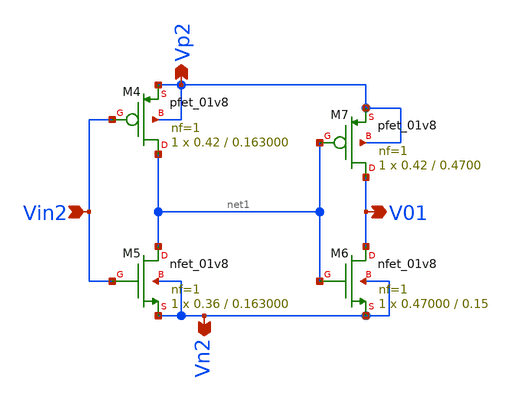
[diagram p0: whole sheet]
** sch_path: xschem/Vth_sch/Symbol/th01_2.sch
**.subckt th01_2 Vn2 Vp2 Vin2 V01
*.opin Vn2
*.opin Vp2
*.ipin Vin2
*.opin V01
XM7 V01 net1 Vp2 Vp2 sky130_fd_pr__pfet_01v8 L=0.4700 W=0.42 nf=1 ad='int((nf+1)/2) * W/nf * 0.29' as='int((nf+2)/2) * W/nf * 0.29'
+ pd='2*int((nf+1)/2) * (W/nf + 0.29)' ps='2*int((nf+2)/2) * (W/nf + 0.29)' nrd='0.29 / W' nrs='0.29 / W'
+ sa=0 sb=0 sd=0 mult=1 m=1
XM6 V01 net1 Vn2 Vn2 sky130_fd_pr__nfet_01v8 L=0.15 W=0.47000 nf=1 ad='int((nf+1)/2) * W/nf * 0.29' as='int((nf+2)/2) * W/nf * 0.29'
+ pd='2*int((nf+1)/2) * (W/nf + 0.29)' ps='2*int((nf+2)/2) * (W/nf + 0.29)' nrd='0.29 / W' nrs='0.29 / W'
+ sa=0 sb=0 sd=0 mult=1 m=1
XM4 net1 Vin2 Vp2 Vp2 sky130_fd_pr__pfet_01v8 L=0.163000 W=0.42 nf=1 ad='int((nf+1)/2) * W/nf * 0.29'
+ as='int((nf+2)/2) * W/nf * 0.29' pd='2*int((nf+1)/2) * (W/nf + 0.29)' ps='2*int((nf+2)/2) * (W/nf + 0.29)'
+ nrd='0.29 / W' nrs='0.29 / W' sa=0 sb=0 sd=0 mult=1 m=1
XM5 net1 Vin2 Vn2 Vn2 sky130_fd_pr__nfet_01v8 L=0.163000 W=0.36 nf=1 ad='int((nf+1)/2) * W/nf * 0.29'
+ as='int((nf+2)/2) * W/nf * 0.29' pd='2*int((nf+1)/2) * (W/nf + 0.29)' ps='2*int((nf+2)/2) * (W/nf + 0.29)'
+ nrd='0.29 / W' nrs='0.29 / W' sa=0 sb=0 sd=0 mult=1 m=1
**.ends
.end
